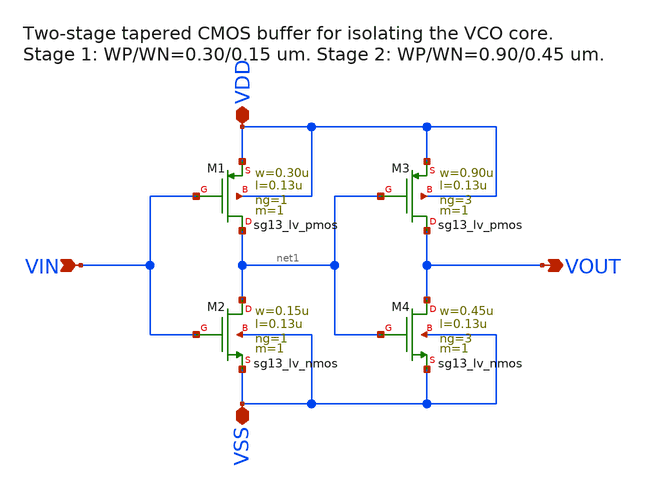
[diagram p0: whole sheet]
** sch_path: macros/pll_analog/schematic/xschem/vco_buffer.sch
**.subckt vco_buffer VIN VOUT VDD VSS
*.ipin VIN
*.opin VOUT
*.iopin VDD
*.iopin VSS
XM1 net1 VIN VDD VDD sg13_lv_pmos w=0.30u l=0.13u ng=1 m=1 mm_ok=1
XM2 net1 VIN VSS VSS sg13_lv_nmos w=0.15u l=0.13u ng=1 m=1 mm_ok=1
XM3 VOUT net1 VDD VDD sg13_lv_pmos w=0.90u l=0.13u ng=3 m=1 mm_ok=1
XM4 VOUT net1 VSS VSS sg13_lv_nmos w=0.45u l=0.13u ng=3 m=1 mm_ok=1
**.ends
.end
